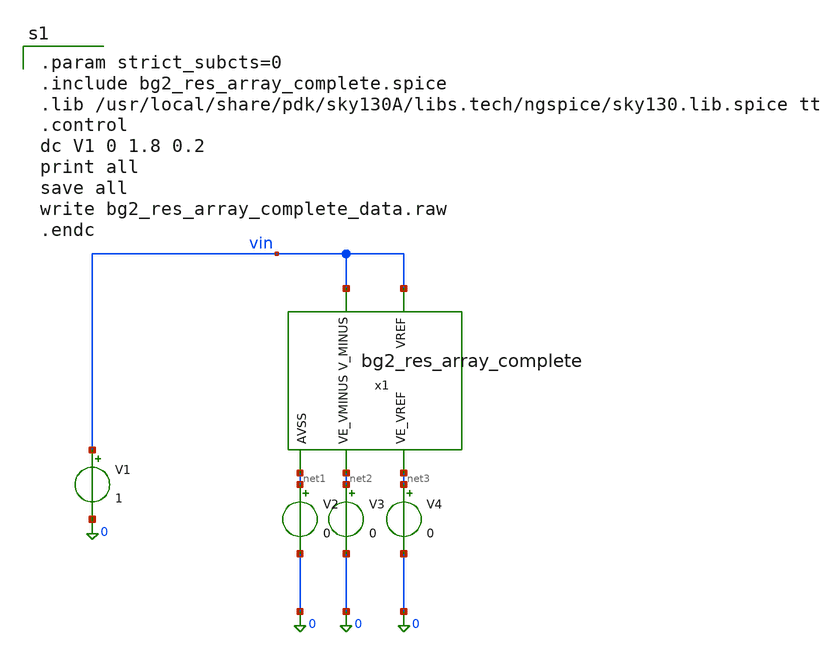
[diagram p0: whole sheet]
** sch_path: gds/bg2_res_array_complete_tb.sch
**.subckt bg2_res_array_complete_tb
V1 vin 0 1
x1 vin vin net1 net3 net2 bg2_res_array_complete
V2 net1 0 0
V3 net2 0 0
V4 net3 0 0
**** begin user architecture code

.param strict_subcts=0
.include bg2_res_array_complete.spice
.lib /usr/local/share/pdk/sky130A/libs.tech/ngspice/sky130.lib.spice tt
.control
dc V1 0 1.8 0.2
print all
save all
write bg2_res_array_complete_data.raw
.endc

**** end user architecture code
**.ends
.end
